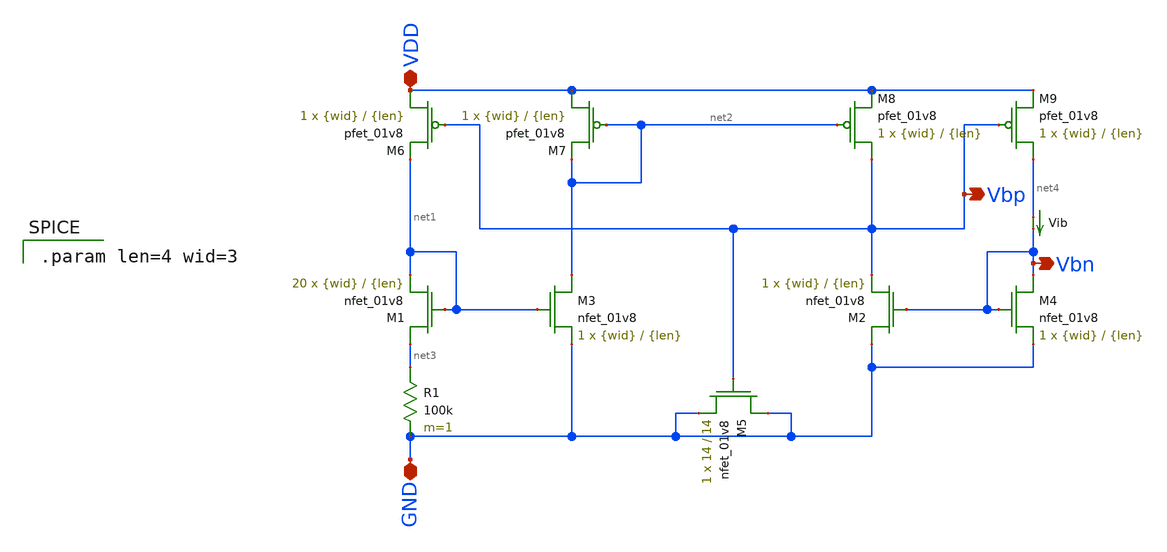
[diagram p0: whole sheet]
** sch_path: mp3/Reference Designs/bias_gen.sch
**.subckt bias_gen GND VDD Vbn Vbp
*.iopin GND
*.iopin VDD
*.opin Vbn
*.opin Vbp
XM1 net3 net1 net1 GND sky130_fd_pr__nfet_01v8 L={len} W={wid} nf=1 ad='int((nf+1)/2) * W/nf * 0.29'
+ as='int((nf+2)/2) * W/nf * 0.29' pd='2*int((nf+1)/2) * (W/nf + 0.29)' ps='2*int((nf+2)/2) * (W/nf + 0.29)'
+ nrd='0.29 / W' nrs='0.29 / W' sa=0 sb=0 sd=0 mult=20 m=20
XM4 Vbn Vbn GND GND sky130_fd_pr__nfet_01v8 L={len} W={wid} nf=1 ad='int((nf+1)/2) * W/nf * 0.29' as='int((nf+2)/2) * W/nf * 0.29'
+ pd='2*int((nf+1)/2) * (W/nf + 0.29)' ps='2*int((nf+2)/2) * (W/nf + 0.29)' nrd='0.29 / W' nrs='0.29 / W'
+ sa=0 sb=0 sd=0 mult=1 m=1
XM5 GND Vbp GND GND sky130_fd_pr__nfet_01v8 L=14 W=14 nf=1 ad='int((nf+1)/2) * W/nf * 0.29' as='int((nf+2)/2) * W/nf * 0.29'
+ pd='2*int((nf+1)/2) * (W/nf + 0.29)' ps='2*int((nf+2)/2) * (W/nf + 0.29)' nrd='0.29 / W' nrs='0.29 / W'
+ sa=0 sb=0 sd=0 mult=1 m=1
XM6 VDD Vbp net1 VDD sky130_fd_pr__pfet_01v8 L={len} W={wid} nf=1 ad='int((nf+1)/2) * W/nf * 0.29' as='int((nf+2)/2) * W/nf * 0.29'
+ pd='2*int((nf+1)/2) * (W/nf + 0.29)' ps='2*int((nf+2)/2) * (W/nf + 0.29)' nrd='0.29 / W' nrs='0.29 / W'
+ sa=0 sb=0 sd=0 mult=1 m=1
R1 net3 GND 100k m=1
XM2 GND Vbn Vbp GND sky130_fd_pr__nfet_01v8 L={len} W={wid} nf=1 ad='int((nf+1)/2) * W/nf * 0.29' as='int((nf+2)/2) * W/nf * 0.29'
+ pd='2*int((nf+1)/2) * (W/nf + 0.29)' ps='2*int((nf+2)/2) * (W/nf + 0.29)' nrd='0.29 / W' nrs='0.29 / W'
+ sa=0 sb=0 sd=0 mult=1 m=1
XM3 net2 net1 GND GND sky130_fd_pr__nfet_01v8 L={len} W={wid} nf=1 ad='int((nf+1)/2) * W/nf * 0.29' as='int((nf+2)/2) * W/nf * 0.29'
+ pd='2*int((nf+1)/2) * (W/nf + 0.29)' ps='2*int((nf+2)/2) * (W/nf + 0.29)' nrd='0.29 / W' nrs='0.29 / W'
+ sa=0 sb=0 sd=0 mult=1 m=1
XM7 VDD net2 net2 VDD sky130_fd_pr__pfet_01v8 L={len} W={wid} nf=1 ad='int((nf+1)/2) * W/nf * 0.29' as='int((nf+2)/2) * W/nf * 0.29'
+ pd='2*int((nf+1)/2) * (W/nf + 0.29)' ps='2*int((nf+2)/2) * (W/nf + 0.29)' nrd='0.29 / W' nrs='0.29 / W'
+ sa=0 sb=0 sd=0 mult=1 m=1
XM8 Vbp net2 VDD VDD sky130_fd_pr__pfet_01v8 L={len} W={wid} nf=1 ad='int((nf+1)/2) * W/nf * 0.29' as='int((nf+2)/2) * W/nf * 0.29'
+ pd='2*int((nf+1)/2) * (W/nf + 0.29)' ps='2*int((nf+2)/2) * (W/nf + 0.29)' nrd='0.29 / W' nrs='0.29 / W'
+ sa=0 sb=0 sd=0 mult=1 m=1
XM9 net4 Vbp VDD VDD sky130_fd_pr__pfet_01v8 L={len} W={wid} nf=1 ad='int((nf+1)/2) * W/nf * 0.29' as='int((nf+2)/2) * W/nf * 0.29'
+ pd='2*int((nf+1)/2) * (W/nf + 0.29)' ps='2*int((nf+2)/2) * (W/nf + 0.29)' nrd='0.29 / W' nrs='0.29 / W'
+ sa=0 sb=0 sd=0 mult=1 m=1
Vib net4 Vbn 0
.save i(vib)
**** begin user architecture code

.param len=4 wid=3

**** end user architecture code
**.ends
.end
